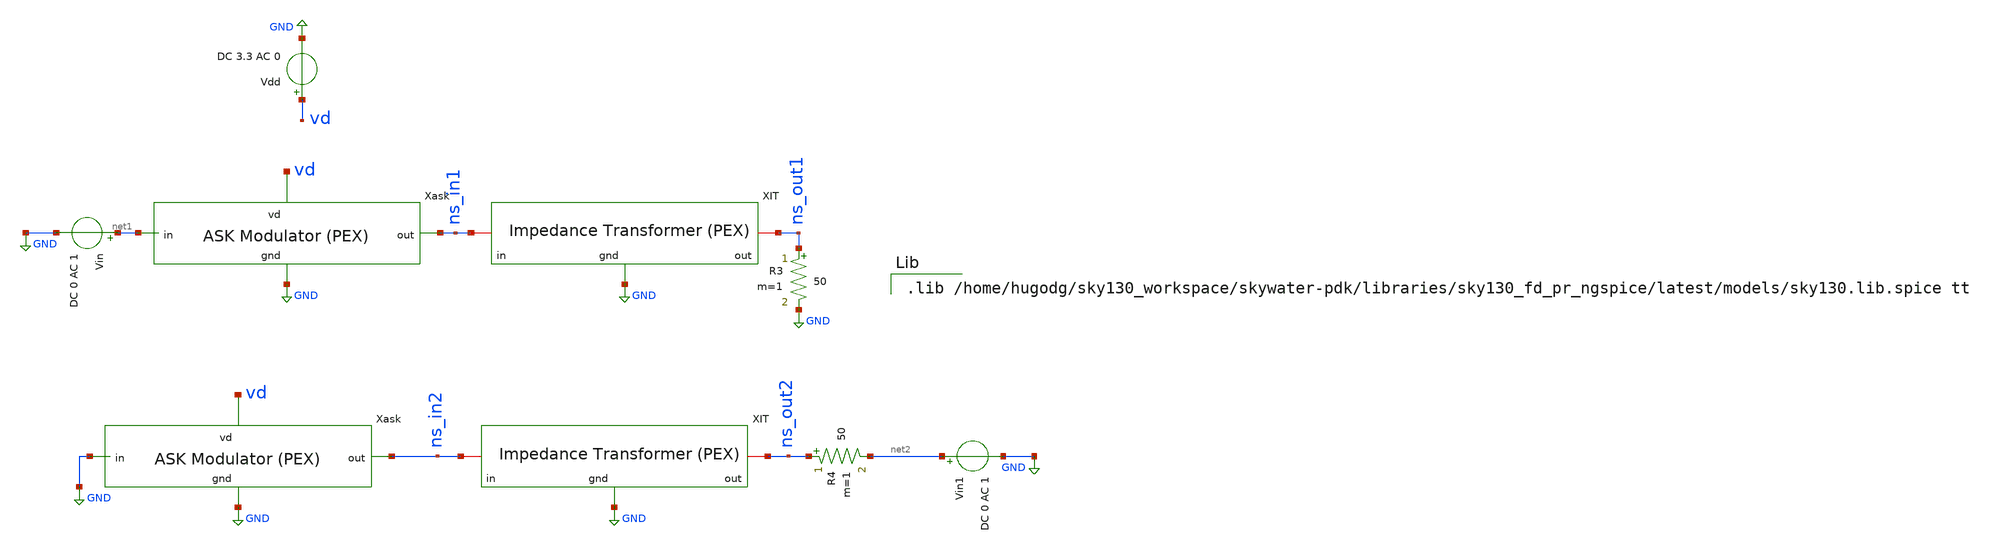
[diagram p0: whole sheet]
** sch_path: impedance-transformer/xschem/impedance-transformer-pex_tb-ac.sch
**.subckt impedance-transformer-pex_tb-ac
Vin net1 GND DC 0 AC 1
Vin1 net2 GND DC 0 AC 1
R3 ns_out1 GND 50 m=1
R4 ns_out2 net2 50 m=1
Vdd vd GND DC 3.3 AC 0
xask1 vd ns_in1 net1 GND ask-modulator-pex
xask2 vd ns_in2 GND GND ask-modulator-pex
xit1 ns_in1 ns_out1 GND impedance-transformer-pex
xit2 ns_in2 ns_out2 GND impedance-transformer-pex
**** begin user architecture code



.ac lin 1MEG 2G 4G
.control
destroy all
set units=degrees
run

set color0=white
set color1=black

let z0=50

* Find two S parameters from test circuit
let s_in1 = v(ns_in1)
let s_out1 = v(ns_out1)
let s_in2 = v(ns_in2)
let s_out2 = v(ns_out2)

* Extract Y parameters
*let StoYDelS = ((1+s_in1)*(1+s_out2)-s_out1*s_in2)*z0
*let y_in1 = ((1+s_out2)*(1-s_in1)+s_out1*s_in2/StoYDelS
*let y_out1=-2*s_out1/StoYDelS
*let y_in2=-2*s_in2/StoYDelS
*let y_out2 = ((1+s_in1)*(1-s_out2)+s_out1+s_in2)/StoYDelS

* Extract Z parameters
let StoZDelS = ((1-s_in1)*(1-s_out2)-s_out1*s_in2)/z0
let z_in1 = ((1+s_in1)*(1-s_out2)+s_out1*s_in2)/StoZDelS
let z_out1 = 2*s_out1/StoZDelS
let z_in2 = 2*s_in2/StoZDelS
let z_out2=((1-s_in1)*(1+s_out2)+s_out1*s_in2)/StoZDelS

*plot z_in1
*plot ph(z_in1)
plot z_out1
plot ph(z_out1)
plot z_out1 xlimit 2.4G 2.5G
.endc


.lib /home/hugodg/sky130_workspace/skywater-pdk/libraries/sky130_fd_pr_ngspice/latest/models/sky130.lib.spice tt

**** end user architecture code
**.ends
.GLOBAL GND
.end
